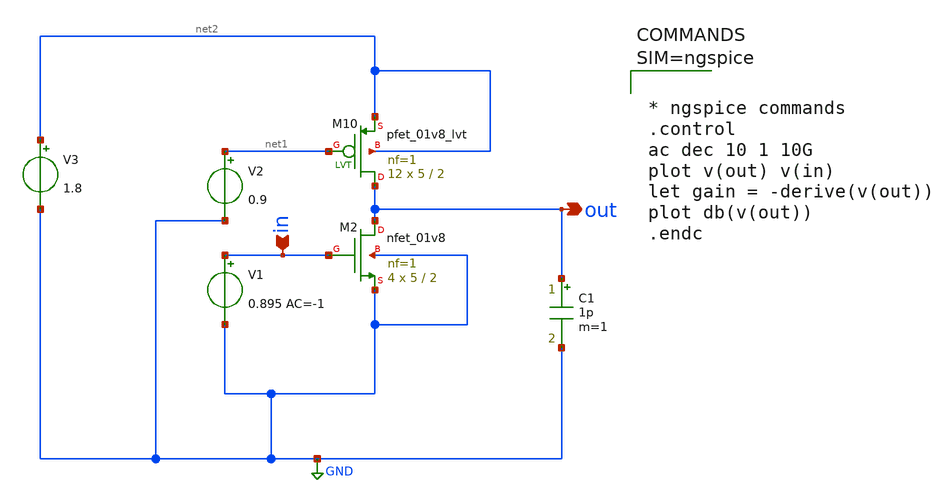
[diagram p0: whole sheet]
** sch_path: xschem/inv_ac.sch
**.subckt inv_ac out in
*.opin out
*.ipin in
XM10 out net1 net2 net2 sky130_fd_pr__pfet_01v8_lvt L=2 W=5 nf=1 ad='int((1 + 1)/2) * 5 / 1 * 0.29' as='int((1 + 2)/2) * 5 / 1 * 0.29'
+ pd='2*int((1 + 1)/2) * (5 / 1 + 0.29)' ps='2*int((1 + 2)/2) * (5 / 1 + 0.29)' nrd='0.29 / 5 ' nrs='0.29 / 5 '
+ sa=0 sb=0 sd=0 mult=12 m=12
XM2 out in GND GND sky130_fd_pr__nfet_01v8 L=2 W=5 nf=1 ad='int((1 + 1)/2) * 5 / 1 * 0.29' as='int((1 + 2)/2) * 5 / 1 * 0.29'
+ pd='2*int((1 + 1)/2) * (5 / 1 + 0.29)' ps='2*int((1 + 2)/2) * (5 / 1 + 0.29)' nrd='0.29 / 5 ' nrs='0.29 / 5 '
+ sa=0 sb=0 sd=0 mult=4 m=4
V1 in GND 0.895 AC=-1
C1 out GND 1p m=1
V2 net1 GND 0.9
V3 net2 GND 1.8
**** begin user architecture code

** opencircuitdesign pdks install
.lib $::SKYWATER_MODELS/sky130.lib.spice tt




* ngspice commands
.control
ac dec 10 1 10G
plot v(out) v(in)
let gain = -derive(v(out))
plot db(v(out))
.endc



**** end user architecture code
**.ends
.GLOBAL GND
.end
